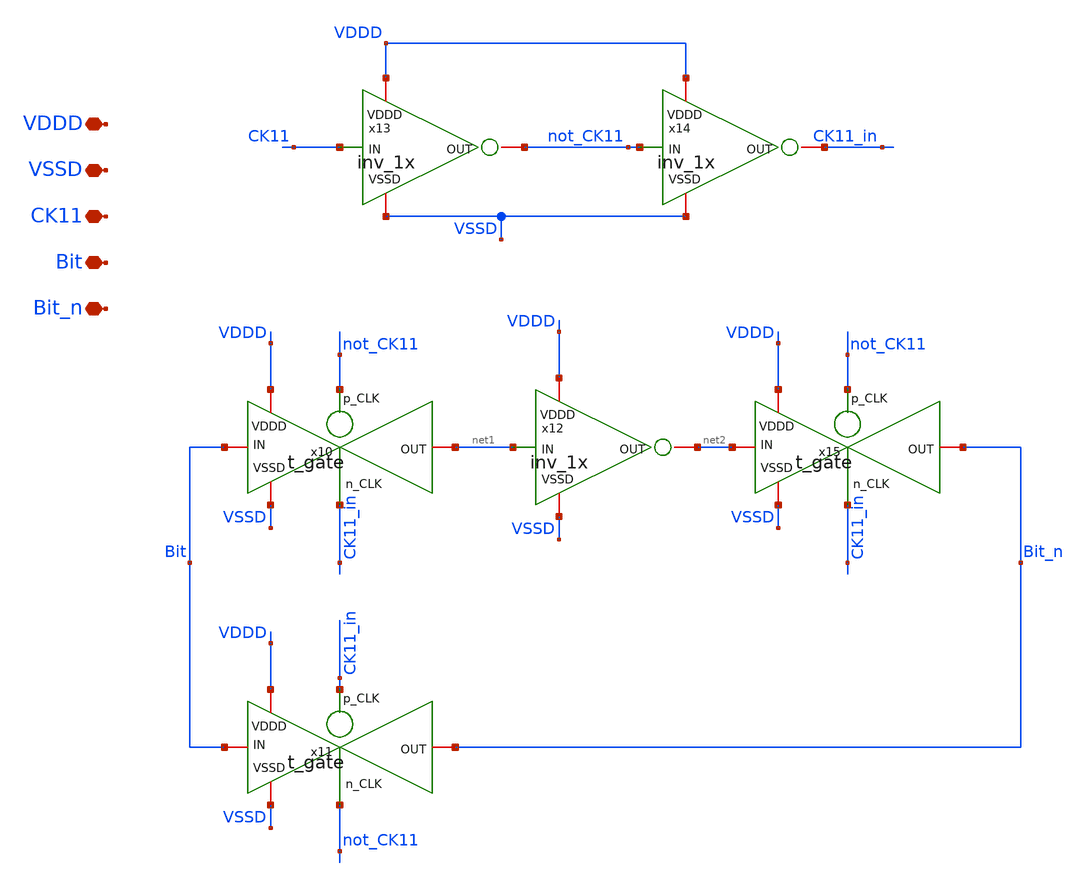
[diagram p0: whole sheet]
** sch_path: SAR_ADC/SAR_Asynchronous_Logic/xschem/neg_bottom_plate.sch
**.subckt neg_bottom_plate VDDD VSSD CK11 Bit Bit_n
*.iopin VDDD
*.iopin VSSD
*.iopin CK11
*.iopin Bit
*.iopin Bit_n
x10 not_CK11 VDDD Bit net1 VSSD CK11_in t_gate
x11 CK11_in VDDD Bit Bit_n VSSD not_CK11 t_gate
x12 VDDD net1 net2 VSSD inv_1x
x13 VDDD CK11 not_CK11 VSSD inv_1x
x14 VDDD not_CK11 CK11_in VSSD inv_1x
x15 not_CK11 VDDD net2 Bit_n VSSD CK11_in t_gate
**.ends
.end
